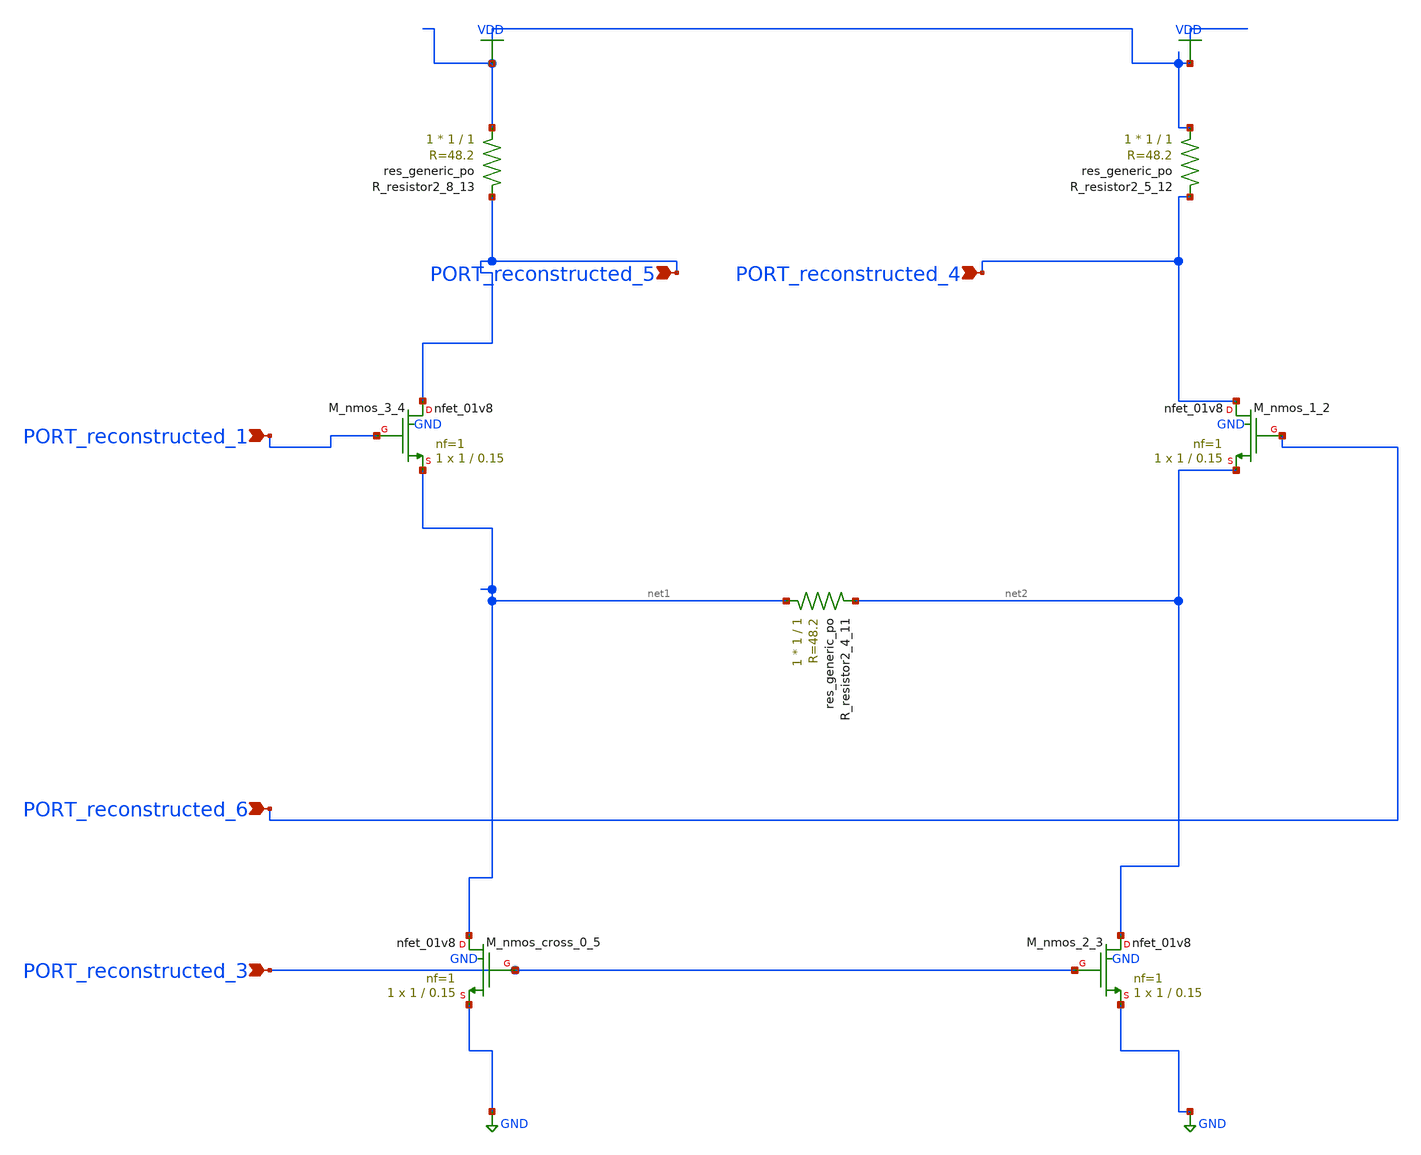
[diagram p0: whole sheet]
** sch_path: schematics/AMSNet/531.sch
**.subckt 531 PORT_reconstructed_1 PORT_reconstructed_4 PORT_reconstructed_5 PORT_reconstructed_6
*+ PORT_reconstructed_3
*.ipin PORT_reconstructed_1
*.ipin PORT_reconstructed_4
*.ipin PORT_reconstructed_5
*.ipin PORT_reconstructed_6
*.ipin PORT_reconstructed_3
XM_nmos_1_2 PORT_reconstructed_4 PORT_reconstructed_6 net2 GND sky130_fd_pr__nfet_01v8 L=0.15 W=1 nf=1
+ ad='int((1 + 1)/2) * 1 / 1 * 0.29' as='int((1 + 2)/2) * 1 / 1 * 0.29' pd='2*int((1 + 1)/2) * (1 / 1 + 0.29)'
+ ps='2*int((1 + 2)/2) * (1 / 1 + 0.29)' nrd='0.29 / 1 ' nrs='0.29 / 1 ' sa=0 sb=0 sd=0 mult=1 m=1
XM_nmos_2_3 net2 PORT_reconstructed_3 GND GND sky130_fd_pr__nfet_01v8 L=0.15 W=1 nf=1 ad='int((1 + 1)/2) * 1 / 1 * 0.29'
+ as='int((1 + 2)/2) * 1 / 1 * 0.29' pd='2*int((1 + 1)/2) * (1 / 1 + 0.29)' ps='2*int((1 + 2)/2) * (1 / 1 + 0.29)'
+ nrd='0.29 / 1 ' nrs='0.29 / 1 ' sa=0 sb=0 sd=0 mult=1 m=1
XM_nmos_3_4 PORT_reconstructed_5 PORT_reconstructed_1 net1 GND sky130_fd_pr__nfet_01v8 L=0.15 W=1 nf=1
+ ad='int((1 + 1)/2) * 1 / 1 * 0.29' as='int((1 + 2)/2) * 1 / 1 * 0.29' pd='2*int((1 + 1)/2) * (1 / 1 + 0.29)'
+ ps='2*int((1 + 2)/2) * (1 / 1 + 0.29)' nrd='0.29 / 1 ' nrs='0.29 / 1 ' sa=0 sb=0 sd=0 mult=1 m=1
XM_nmos_cross_0_5 net1 PORT_reconstructed_3 GND GND sky130_fd_pr__nfet_01v8 L=0.15 W=1 nf=1 ad='int((1 + 1)/2) * 1 / 1 * 0.29'
+ as='int((1 + 2)/2) * 1 / 1 * 0.29' pd='2*int((1 + 1)/2) * (1 / 1 + 0.29)' ps='2*int((1 + 2)/2) * (1 / 1 + 0.29)'
+ nrd='0.29 / 1 ' nrs='0.29 / 1 ' sa=0 sb=0 sd=0 mult=1 m=1
XR_resistor2_4_11 net1 net2 sky130_fd_pr__res_generic_po W=1 L=1 m=1
XR_resistor2_5_12 VDD PORT_reconstructed_4 sky130_fd_pr__res_generic_po W=1 L=1 m=1
XR_resistor2_8_13 VDD PORT_reconstructed_5 sky130_fd_pr__res_generic_po W=1 L=1 m=1
**.ends
.GLOBAL GND
.GLOBAL VDD
.end
